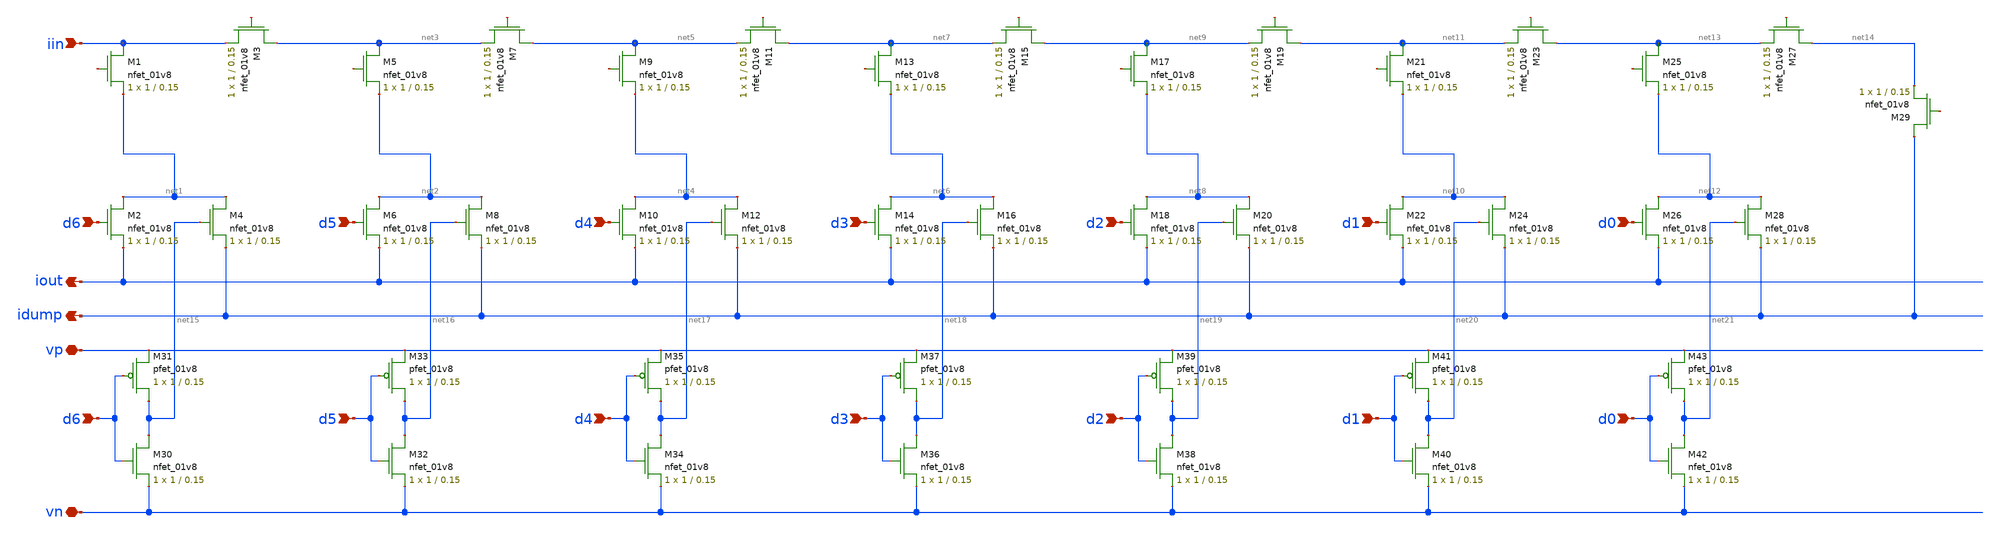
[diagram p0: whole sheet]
** sch_path: schematic/ladder.sch
**.subckt ladder iout idump iin d6 d5 d4 d3 d2 d1 d0 vn vp d6 d5 d4 d3 d2 d1 d0
*.opin iout
*.opin idump
*.ipin iin
*.ipin d6
*.ipin d5
*.ipin d4
*.ipin d3
*.ipin d2
*.ipin d1
*.ipin d0
*.iopin vn
*.iopin vp
*.ipin d6
*.ipin d5
*.ipin d4
*.ipin d3
*.ipin d2
*.ipin d1
*.ipin d0
XM1 iin net22 net1 GND sky130_fd_pr__nfet_01v8 L=0.15 W=1 nf=1 ad='int((nf+1)/2) * W/nf * 0.29' as='int((nf+2)/2) * W/nf * 0.29'
+ pd='2*int((nf+1)/2) * (W/nf + 0.29)' ps='2*int((nf+2)/2) * (W/nf + 0.29)' nrd='0.29 / W' nrs='0.29 / W'
+ sa=0 sb=0 sd=0 mult=1 m=1
XM2 net1 d6 iout GND sky130_fd_pr__nfet_01v8 L=0.15 W=1 nf=1 ad='int((nf+1)/2) * W/nf * 0.29' as='int((nf+2)/2) * W/nf * 0.29'
+ pd='2*int((nf+1)/2) * (W/nf + 0.29)' ps='2*int((nf+2)/2) * (W/nf + 0.29)' nrd='0.29 / W' nrs='0.29 / W'
+ sa=0 sb=0 sd=0 mult=1 m=1
XM3 net3 net23 iin GND sky130_fd_pr__nfet_01v8 L=0.15 W=1 nf=1 ad='int((nf+1)/2) * W/nf * 0.29' as='int((nf+2)/2) * W/nf * 0.29'
+ pd='2*int((nf+1)/2) * (W/nf + 0.29)' ps='2*int((nf+2)/2) * (W/nf + 0.29)' nrd='0.29 / W' nrs='0.29 / W'
+ sa=0 sb=0 sd=0 mult=1 m=1
XM4 net1 net15 idump GND sky130_fd_pr__nfet_01v8 L=0.15 W=1 nf=1 ad='int((nf+1)/2) * W/nf * 0.29' as='int((nf+2)/2) * W/nf * 0.29'
+ pd='2*int((nf+1)/2) * (W/nf + 0.29)' ps='2*int((nf+2)/2) * (W/nf + 0.29)' nrd='0.29 / W' nrs='0.29 / W'
+ sa=0 sb=0 sd=0 mult=1 m=1
XM5 net3 net24 net2 GND sky130_fd_pr__nfet_01v8 L=0.15 W=1 nf=1 ad='int((nf+1)/2) * W/nf * 0.29' as='int((nf+2)/2) * W/nf * 0.29'
+ pd='2*int((nf+1)/2) * (W/nf + 0.29)' ps='2*int((nf+2)/2) * (W/nf + 0.29)' nrd='0.29 / W' nrs='0.29 / W'
+ sa=0 sb=0 sd=0 mult=1 m=1
XM6 net2 d5 iout GND sky130_fd_pr__nfet_01v8 L=0.15 W=1 nf=1 ad='int((nf+1)/2) * W/nf * 0.29' as='int((nf+2)/2) * W/nf * 0.29'
+ pd='2*int((nf+1)/2) * (W/nf + 0.29)' ps='2*int((nf+2)/2) * (W/nf + 0.29)' nrd='0.29 / W' nrs='0.29 / W'
+ sa=0 sb=0 sd=0 mult=1 m=1
XM7 net5 net25 net3 GND sky130_fd_pr__nfet_01v8 L=0.15 W=1 nf=1 ad='int((nf+1)/2) * W/nf * 0.29' as='int((nf+2)/2) * W/nf * 0.29'
+ pd='2*int((nf+1)/2) * (W/nf + 0.29)' ps='2*int((nf+2)/2) * (W/nf + 0.29)' nrd='0.29 / W' nrs='0.29 / W'
+ sa=0 sb=0 sd=0 mult=1 m=1
XM8 net2 net16 idump GND sky130_fd_pr__nfet_01v8 L=0.15 W=1 nf=1 ad='int((nf+1)/2) * W/nf * 0.29' as='int((nf+2)/2) * W/nf * 0.29'
+ pd='2*int((nf+1)/2) * (W/nf + 0.29)' ps='2*int((nf+2)/2) * (W/nf + 0.29)' nrd='0.29 / W' nrs='0.29 / W'
+ sa=0 sb=0 sd=0 mult=1 m=1
XM9 net5 net26 net4 GND sky130_fd_pr__nfet_01v8 L=0.15 W=1 nf=1 ad='int((nf+1)/2) * W/nf * 0.29' as='int((nf+2)/2) * W/nf * 0.29'
+ pd='2*int((nf+1)/2) * (W/nf + 0.29)' ps='2*int((nf+2)/2) * (W/nf + 0.29)' nrd='0.29 / W' nrs='0.29 / W'
+ sa=0 sb=0 sd=0 mult=1 m=1
XM10 net4 d4 iout GND sky130_fd_pr__nfet_01v8 L=0.15 W=1 nf=1 ad='int((nf+1)/2) * W/nf * 0.29' as='int((nf+2)/2) * W/nf * 0.29'
+ pd='2*int((nf+1)/2) * (W/nf + 0.29)' ps='2*int((nf+2)/2) * (W/nf + 0.29)' nrd='0.29 / W' nrs='0.29 / W'
+ sa=0 sb=0 sd=0 mult=1 m=1
XM11 net7 net27 net5 GND sky130_fd_pr__nfet_01v8 L=0.15 W=1 nf=1 ad='int((nf+1)/2) * W/nf * 0.29' as='int((nf+2)/2) * W/nf * 0.29'
+ pd='2*int((nf+1)/2) * (W/nf + 0.29)' ps='2*int((nf+2)/2) * (W/nf + 0.29)' nrd='0.29 / W' nrs='0.29 / W'
+ sa=0 sb=0 sd=0 mult=1 m=1
XM12 net4 net17 idump GND sky130_fd_pr__nfet_01v8 L=0.15 W=1 nf=1 ad='int((nf+1)/2) * W/nf * 0.29' as='int((nf+2)/2) * W/nf * 0.29'
+ pd='2*int((nf+1)/2) * (W/nf + 0.29)' ps='2*int((nf+2)/2) * (W/nf + 0.29)' nrd='0.29 / W' nrs='0.29 / W'
+ sa=0 sb=0 sd=0 mult=1 m=1
XM13 net7 net28 net6 GND sky130_fd_pr__nfet_01v8 L=0.15 W=1 nf=1 ad='int((nf+1)/2) * W/nf * 0.29' as='int((nf+2)/2) * W/nf * 0.29'
+ pd='2*int((nf+1)/2) * (W/nf + 0.29)' ps='2*int((nf+2)/2) * (W/nf + 0.29)' nrd='0.29 / W' nrs='0.29 / W'
+ sa=0 sb=0 sd=0 mult=1 m=1
XM14 net6 d3 iout GND sky130_fd_pr__nfet_01v8 L=0.15 W=1 nf=1 ad='int((nf+1)/2) * W/nf * 0.29' as='int((nf+2)/2) * W/nf * 0.29'
+ pd='2*int((nf+1)/2) * (W/nf + 0.29)' ps='2*int((nf+2)/2) * (W/nf + 0.29)' nrd='0.29 / W' nrs='0.29 / W'
+ sa=0 sb=0 sd=0 mult=1 m=1
XM15 net9 net29 net7 GND sky130_fd_pr__nfet_01v8 L=0.15 W=1 nf=1 ad='int((nf+1)/2) * W/nf * 0.29' as='int((nf+2)/2) * W/nf * 0.29'
+ pd='2*int((nf+1)/2) * (W/nf + 0.29)' ps='2*int((nf+2)/2) * (W/nf + 0.29)' nrd='0.29 / W' nrs='0.29 / W'
+ sa=0 sb=0 sd=0 mult=1 m=1
XM16 net6 net18 idump GND sky130_fd_pr__nfet_01v8 L=0.15 W=1 nf=1 ad='int((nf+1)/2) * W/nf * 0.29' as='int((nf+2)/2) * W/nf * 0.29'
+ pd='2*int((nf+1)/2) * (W/nf + 0.29)' ps='2*int((nf+2)/2) * (W/nf + 0.29)' nrd='0.29 / W' nrs='0.29 / W'
+ sa=0 sb=0 sd=0 mult=1 m=1
XM17 net9 net30 net8 GND sky130_fd_pr__nfet_01v8 L=0.15 W=1 nf=1 ad='int((nf+1)/2) * W/nf * 0.29' as='int((nf+2)/2) * W/nf * 0.29'
+ pd='2*int((nf+1)/2) * (W/nf + 0.29)' ps='2*int((nf+2)/2) * (W/nf + 0.29)' nrd='0.29 / W' nrs='0.29 / W'
+ sa=0 sb=0 sd=0 mult=1 m=1
XM18 net8 d2 iout GND sky130_fd_pr__nfet_01v8 L=0.15 W=1 nf=1 ad='int((nf+1)/2) * W/nf * 0.29' as='int((nf+2)/2) * W/nf * 0.29'
+ pd='2*int((nf+1)/2) * (W/nf + 0.29)' ps='2*int((nf+2)/2) * (W/nf + 0.29)' nrd='0.29 / W' nrs='0.29 / W'
+ sa=0 sb=0 sd=0 mult=1 m=1
XM19 net11 net31 net9 GND sky130_fd_pr__nfet_01v8 L=0.15 W=1 nf=1 ad='int((nf+1)/2) * W/nf * 0.29' as='int((nf+2)/2) * W/nf * 0.29'
+ pd='2*int((nf+1)/2) * (W/nf + 0.29)' ps='2*int((nf+2)/2) * (W/nf + 0.29)' nrd='0.29 / W' nrs='0.29 / W'
+ sa=0 sb=0 sd=0 mult=1 m=1
XM20 net8 net19 idump GND sky130_fd_pr__nfet_01v8 L=0.15 W=1 nf=1 ad='int((nf+1)/2) * W/nf * 0.29' as='int((nf+2)/2) * W/nf * 0.29'
+ pd='2*int((nf+1)/2) * (W/nf + 0.29)' ps='2*int((nf+2)/2) * (W/nf + 0.29)' nrd='0.29 / W' nrs='0.29 / W'
+ sa=0 sb=0 sd=0 mult=1 m=1
XM21 net11 net32 net10 GND sky130_fd_pr__nfet_01v8 L=0.15 W=1 nf=1 ad='int((nf+1)/2) * W/nf * 0.29' as='int((nf+2)/2) * W/nf * 0.29'
+ pd='2*int((nf+1)/2) * (W/nf + 0.29)' ps='2*int((nf+2)/2) * (W/nf + 0.29)' nrd='0.29 / W' nrs='0.29 / W'
+ sa=0 sb=0 sd=0 mult=1 m=1
XM22 net10 d1 iout GND sky130_fd_pr__nfet_01v8 L=0.15 W=1 nf=1 ad='int((nf+1)/2) * W/nf * 0.29' as='int((nf+2)/2) * W/nf * 0.29'
+ pd='2*int((nf+1)/2) * (W/nf + 0.29)' ps='2*int((nf+2)/2) * (W/nf + 0.29)' nrd='0.29 / W' nrs='0.29 / W'
+ sa=0 sb=0 sd=0 mult=1 m=1
XM23 net13 net33 net11 GND sky130_fd_pr__nfet_01v8 L=0.15 W=1 nf=1 ad='int((nf+1)/2) * W/nf * 0.29' as='int((nf+2)/2) * W/nf * 0.29'
+ pd='2*int((nf+1)/2) * (W/nf + 0.29)' ps='2*int((nf+2)/2) * (W/nf + 0.29)' nrd='0.29 / W' nrs='0.29 / W'
+ sa=0 sb=0 sd=0 mult=1 m=1
XM24 net10 net20 idump GND sky130_fd_pr__nfet_01v8 L=0.15 W=1 nf=1 ad='int((nf+1)/2) * W/nf * 0.29' as='int((nf+2)/2) * W/nf * 0.29'
+ pd='2*int((nf+1)/2) * (W/nf + 0.29)' ps='2*int((nf+2)/2) * (W/nf + 0.29)' nrd='0.29 / W' nrs='0.29 / W'
+ sa=0 sb=0 sd=0 mult=1 m=1
XM25 net13 net34 net12 GND sky130_fd_pr__nfet_01v8 L=0.15 W=1 nf=1 ad='int((nf+1)/2) * W/nf * 0.29' as='int((nf+2)/2) * W/nf * 0.29'
+ pd='2*int((nf+1)/2) * (W/nf + 0.29)' ps='2*int((nf+2)/2) * (W/nf + 0.29)' nrd='0.29 / W' nrs='0.29 / W'
+ sa=0 sb=0 sd=0 mult=1 m=1
XM26 net12 d0 iout GND sky130_fd_pr__nfet_01v8 L=0.15 W=1 nf=1 ad='int((nf+1)/2) * W/nf * 0.29' as='int((nf+2)/2) * W/nf * 0.29'
+ pd='2*int((nf+1)/2) * (W/nf + 0.29)' ps='2*int((nf+2)/2) * (W/nf + 0.29)' nrd='0.29 / W' nrs='0.29 / W'
+ sa=0 sb=0 sd=0 mult=1 m=1
XM27 net14 net35 net13 GND sky130_fd_pr__nfet_01v8 L=0.15 W=1 nf=1 ad='int((nf+1)/2) * W/nf * 0.29' as='int((nf+2)/2) * W/nf * 0.29'
+ pd='2*int((nf+1)/2) * (W/nf + 0.29)' ps='2*int((nf+2)/2) * (W/nf + 0.29)' nrd='0.29 / W' nrs='0.29 / W'
+ sa=0 sb=0 sd=0 mult=1 m=1
XM28 net12 net21 idump GND sky130_fd_pr__nfet_01v8 L=0.15 W=1 nf=1 ad='int((nf+1)/2) * W/nf * 0.29' as='int((nf+2)/2) * W/nf * 0.29'
+ pd='2*int((nf+1)/2) * (W/nf + 0.29)' ps='2*int((nf+2)/2) * (W/nf + 0.29)' nrd='0.29 / W' nrs='0.29 / W'
+ sa=0 sb=0 sd=0 mult=1 m=1
XM29 idump net36 net14 GND sky130_fd_pr__nfet_01v8 L=0.15 W=1 nf=1 ad='int((nf+1)/2) * W/nf * 0.29' as='int((nf+2)/2) * W/nf * 0.29'
+ pd='2*int((nf+1)/2) * (W/nf + 0.29)' ps='2*int((nf+2)/2) * (W/nf + 0.29)' nrd='0.29 / W' nrs='0.29 / W'
+ sa=0 sb=0 sd=0 mult=1 m=1
XM30 net15 d6 vn GND sky130_fd_pr__nfet_01v8 L=0.15 W=1 nf=1 ad='int((nf+1)/2) * W/nf * 0.29' as='int((nf+2)/2) * W/nf * 0.29'
+ pd='2*int((nf+1)/2) * (W/nf + 0.29)' ps='2*int((nf+2)/2) * (W/nf + 0.29)' nrd='0.29 / W' nrs='0.29 / W'
+ sa=0 sb=0 sd=0 mult=1 m=1
XM31 net15 d6 vp VDD sky130_fd_pr__pfet_01v8 L=0.15 W=1 nf=1 ad='int((nf+1)/2) * W/nf * 0.29' as='int((nf+2)/2) * W/nf * 0.29'
+ pd='2*int((nf+1)/2) * (W/nf + 0.29)' ps='2*int((nf+2)/2) * (W/nf + 0.29)' nrd='0.29 / W' nrs='0.29 / W'
+ sa=0 sb=0 sd=0 mult=1 m=1
XM32 net16 d5 vn GND sky130_fd_pr__nfet_01v8 L=0.15 W=1 nf=1 ad='int((nf+1)/2) * W/nf * 0.29' as='int((nf+2)/2) * W/nf * 0.29'
+ pd='2*int((nf+1)/2) * (W/nf + 0.29)' ps='2*int((nf+2)/2) * (W/nf + 0.29)' nrd='0.29 / W' nrs='0.29 / W'
+ sa=0 sb=0 sd=0 mult=1 m=1
XM33 net16 d5 vp VDD sky130_fd_pr__pfet_01v8 L=0.15 W=1 nf=1 ad='int((nf+1)/2) * W/nf * 0.29' as='int((nf+2)/2) * W/nf * 0.29'
+ pd='2*int((nf+1)/2) * (W/nf + 0.29)' ps='2*int((nf+2)/2) * (W/nf + 0.29)' nrd='0.29 / W' nrs='0.29 / W'
+ sa=0 sb=0 sd=0 mult=1 m=1
XM34 net17 d4 vn GND sky130_fd_pr__nfet_01v8 L=0.15 W=1 nf=1 ad='int((nf+1)/2) * W/nf * 0.29' as='int((nf+2)/2) * W/nf * 0.29'
+ pd='2*int((nf+1)/2) * (W/nf + 0.29)' ps='2*int((nf+2)/2) * (W/nf + 0.29)' nrd='0.29 / W' nrs='0.29 / W'
+ sa=0 sb=0 sd=0 mult=1 m=1
XM35 net17 d4 vp VDD sky130_fd_pr__pfet_01v8 L=0.15 W=1 nf=1 ad='int((nf+1)/2) * W/nf * 0.29' as='int((nf+2)/2) * W/nf * 0.29'
+ pd='2*int((nf+1)/2) * (W/nf + 0.29)' ps='2*int((nf+2)/2) * (W/nf + 0.29)' nrd='0.29 / W' nrs='0.29 / W'
+ sa=0 sb=0 sd=0 mult=1 m=1
XM36 net18 d3 vn GND sky130_fd_pr__nfet_01v8 L=0.15 W=1 nf=1 ad='int((nf+1)/2) * W/nf * 0.29' as='int((nf+2)/2) * W/nf * 0.29'
+ pd='2*int((nf+1)/2) * (W/nf + 0.29)' ps='2*int((nf+2)/2) * (W/nf + 0.29)' nrd='0.29 / W' nrs='0.29 / W'
+ sa=0 sb=0 sd=0 mult=1 m=1
XM37 net18 d3 vp VDD sky130_fd_pr__pfet_01v8 L=0.15 W=1 nf=1 ad='int((nf+1)/2) * W/nf * 0.29' as='int((nf+2)/2) * W/nf * 0.29'
+ pd='2*int((nf+1)/2) * (W/nf + 0.29)' ps='2*int((nf+2)/2) * (W/nf + 0.29)' nrd='0.29 / W' nrs='0.29 / W'
+ sa=0 sb=0 sd=0 mult=1 m=1
XM38 net19 d2 vn GND sky130_fd_pr__nfet_01v8 L=0.15 W=1 nf=1 ad='int((nf+1)/2) * W/nf * 0.29' as='int((nf+2)/2) * W/nf * 0.29'
+ pd='2*int((nf+1)/2) * (W/nf + 0.29)' ps='2*int((nf+2)/2) * (W/nf + 0.29)' nrd='0.29 / W' nrs='0.29 / W'
+ sa=0 sb=0 sd=0 mult=1 m=1
XM39 net19 d2 vp VDD sky130_fd_pr__pfet_01v8 L=0.15 W=1 nf=1 ad='int((nf+1)/2) * W/nf * 0.29' as='int((nf+2)/2) * W/nf * 0.29'
+ pd='2*int((nf+1)/2) * (W/nf + 0.29)' ps='2*int((nf+2)/2) * (W/nf + 0.29)' nrd='0.29 / W' nrs='0.29 / W'
+ sa=0 sb=0 sd=0 mult=1 m=1
XM40 net20 d1 vn GND sky130_fd_pr__nfet_01v8 L=0.15 W=1 nf=1 ad='int((nf+1)/2) * W/nf * 0.29' as='int((nf+2)/2) * W/nf * 0.29'
+ pd='2*int((nf+1)/2) * (W/nf + 0.29)' ps='2*int((nf+2)/2) * (W/nf + 0.29)' nrd='0.29 / W' nrs='0.29 / W'
+ sa=0 sb=0 sd=0 mult=1 m=1
XM41 net20 d1 vp VDD sky130_fd_pr__pfet_01v8 L=0.15 W=1 nf=1 ad='int((nf+1)/2) * W/nf * 0.29' as='int((nf+2)/2) * W/nf * 0.29'
+ pd='2*int((nf+1)/2) * (W/nf + 0.29)' ps='2*int((nf+2)/2) * (W/nf + 0.29)' nrd='0.29 / W' nrs='0.29 / W'
+ sa=0 sb=0 sd=0 mult=1 m=1
XM42 net21 d0 vn GND sky130_fd_pr__nfet_01v8 L=0.15 W=1 nf=1 ad='int((nf+1)/2) * W/nf * 0.29' as='int((nf+2)/2) * W/nf * 0.29'
+ pd='2*int((nf+1)/2) * (W/nf + 0.29)' ps='2*int((nf+2)/2) * (W/nf + 0.29)' nrd='0.29 / W' nrs='0.29 / W'
+ sa=0 sb=0 sd=0 mult=1 m=1
XM43 net21 d0 vp VDD sky130_fd_pr__pfet_01v8 L=0.15 W=1 nf=1 ad='int((nf+1)/2) * W/nf * 0.29' as='int((nf+2)/2) * W/nf * 0.29'
+ pd='2*int((nf+1)/2) * (W/nf + 0.29)' ps='2*int((nf+2)/2) * (W/nf + 0.29)' nrd='0.29 / W' nrs='0.29 / W'
+ sa=0 sb=0 sd=0 mult=1 m=1
**.ends
.end
